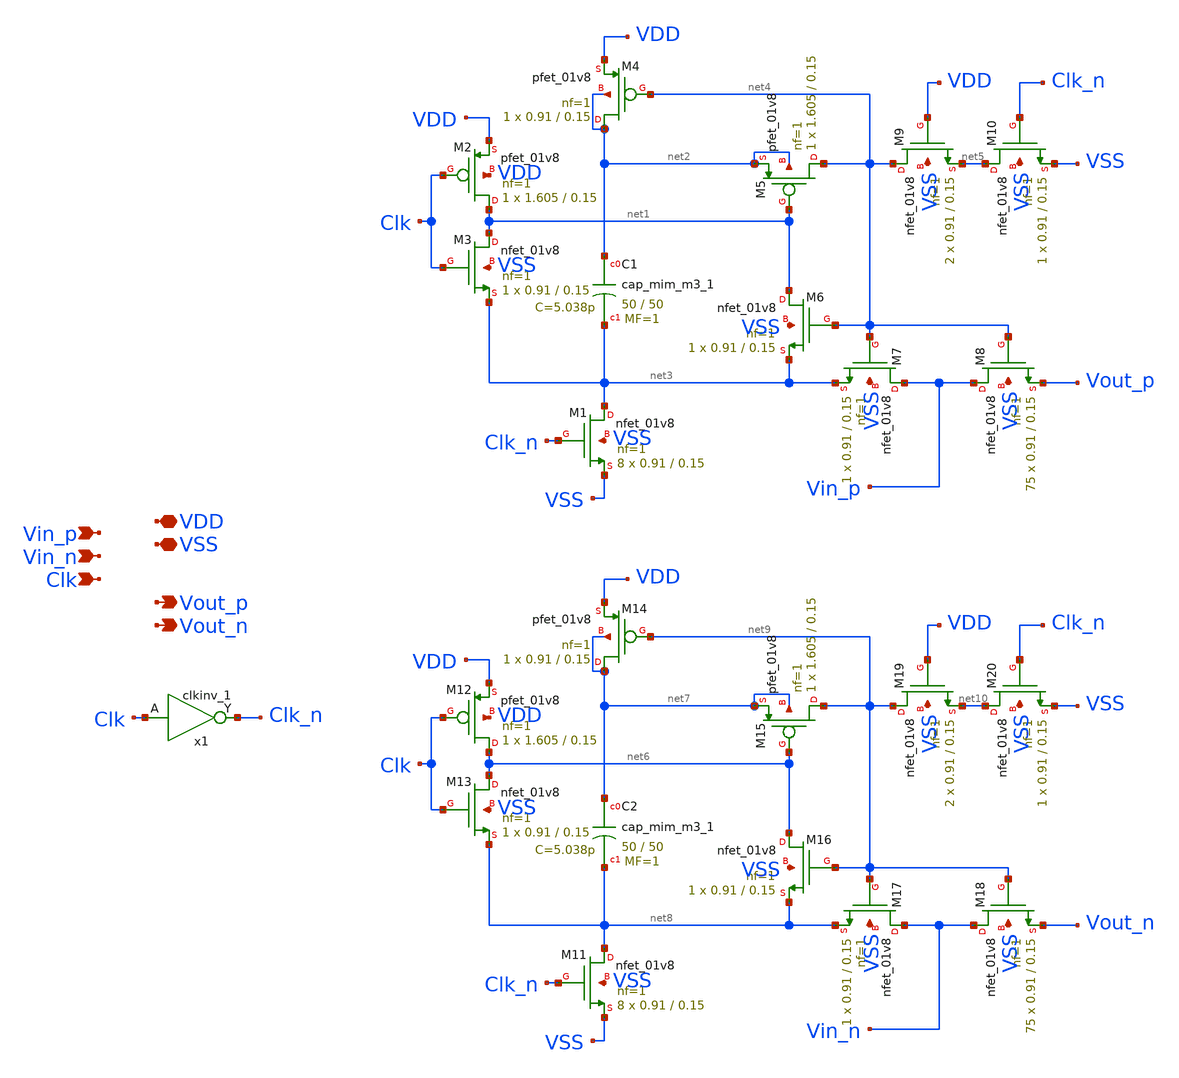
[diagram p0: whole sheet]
** sch_path: xschem/src/bootstrapped_sampling_switch/bootstrapped_sampling_switch.sch
**.subckt bootstrapped_sampling_switch VDD Vin_p Vout_p VSS Vout_n Vin_n Clk
*.iopin VDD
*.ipin Vin_p
*.opin Vout_p
*.iopin VSS
*.opin Vout_n
*.ipin Vin_n
*.ipin Clk
XM1 net3 Clk_n VSS VSS sky130_fd_pr__nfet_01v8 L=0.15 W=0.91 nf=1 ad='int((nf+1)/2) * W/nf * 0.29' as='int((nf+2)/2) * W/nf * 0.29'
+ pd='2*int((nf+1)/2) * (W/nf + 0.29)' ps='2*int((nf+2)/2) * (W/nf + 0.29)' nrd='0.29 / W' nrs='0.29 / W'
+ sa=0 sb=0 sd=0 mult=8 m=8
XM2 net1 Clk VDD VDD sky130_fd_pr__pfet_01v8 L=0.15 W=1.605 nf=1 ad='int((nf+1)/2) * W/nf * 0.29' as='int((nf+2)/2) * W/nf * 0.29'
+ pd='2*int((nf+1)/2) * (W/nf + 0.29)' ps='2*int((nf+2)/2) * (W/nf + 0.29)' nrd='0.29 / W' nrs='0.29 / W'
+ sa=0 sb=0 sd=0 mult=1 m=1
XM3 net1 Clk net3 VSS sky130_fd_pr__nfet_01v8 L=0.15 W=0.91 nf=1 ad='int((nf+1)/2) * W/nf * 0.29' as='int((nf+2)/2) * W/nf * 0.29'
+ pd='2*int((nf+1)/2) * (W/nf + 0.29)' ps='2*int((nf+2)/2) * (W/nf + 0.29)' nrd='0.29 / W' nrs='0.29 / W'
+ sa=0 sb=0 sd=0 mult=1 m=1
XC1 net2 net3 sky130_fd_pr__cap_mim_m3_1 W=50 L=50 MF=1 m=1
XM4 net2 net4 VDD net2 sky130_fd_pr__pfet_01v8 L=0.15 W=0.91 nf=1 ad='int((nf+1)/2) * W/nf * 0.29' as='int((nf+2)/2) * W/nf * 0.29'
+ pd='2*int((nf+1)/2) * (W/nf + 0.29)' ps='2*int((nf+2)/2) * (W/nf + 0.29)' nrd='0.29 / W' nrs='0.29 / W'
+ sa=0 sb=0 sd=0 mult=1 m=1
XM5 net4 net1 net2 net2 sky130_fd_pr__pfet_01v8 L=0.15 W=1.605 nf=1 ad='int((nf+1)/2) * W/nf * 0.29'
+ as='int((nf+2)/2) * W/nf * 0.29' pd='2*int((nf+1)/2) * (W/nf + 0.29)' ps='2*int((nf+2)/2) * (W/nf + 0.29)'
+ nrd='0.29 / W' nrs='0.29 / W' sa=0 sb=0 sd=0 mult=1 m=1
XM6 net1 net4 net3 VSS sky130_fd_pr__nfet_01v8 L=0.15 W=0.91 nf=1 ad='int((nf+1)/2) * W/nf * 0.29' as='int((nf+2)/2) * W/nf * 0.29'
+ pd='2*int((nf+1)/2) * (W/nf + 0.29)' ps='2*int((nf+2)/2) * (W/nf + 0.29)' nrd='0.29 / W' nrs='0.29 / W'
+ sa=0 sb=0 sd=0 mult=1 m=1
XM7 Vin_p net4 net3 VSS sky130_fd_pr__nfet_01v8 L=0.15 W=0.91 nf=1 ad='int((nf+1)/2) * W/nf * 0.29' as='int((nf+2)/2) * W/nf * 0.29'
+ pd='2*int((nf+1)/2) * (W/nf + 0.29)' ps='2*int((nf+2)/2) * (W/nf + 0.29)' nrd='0.29 / W' nrs='0.29 / W'
+ sa=0 sb=0 sd=0 mult=1 m=1
XM8 Vin_p net4 Vout_p VSS sky130_fd_pr__nfet_01v8 L=0.15 W=0.91 nf=1 ad='int((nf+1)/2) * W/nf * 0.29'
+ as='int((nf+2)/2) * W/nf * 0.29' pd='2*int((nf+1)/2) * (W/nf + 0.29)' ps='2*int((nf+2)/2) * (W/nf + 0.29)'
+ nrd='0.29 / W' nrs='0.29 / W' sa=0 sb=0 sd=0 mult=75 m=75
XM9 net4 VDD net5 VSS sky130_fd_pr__nfet_01v8 L=0.15 W=0.91 nf=1 ad='int((nf+1)/2) * W/nf * 0.29' as='int((nf+2)/2) * W/nf * 0.29'
+ pd='2*int((nf+1)/2) * (W/nf + 0.29)' ps='2*int((nf+2)/2) * (W/nf + 0.29)' nrd='0.29 / W' nrs='0.29 / W'
+ sa=0 sb=0 sd=0 mult=2 m=2
XM10 net5 Clk_n VSS VSS sky130_fd_pr__nfet_01v8 L=0.15 W=0.91 nf=1 ad='int((nf+1)/2) * W/nf * 0.29' as='int((nf+2)/2) * W/nf * 0.29'
+ pd='2*int((nf+1)/2) * (W/nf + 0.29)' ps='2*int((nf+2)/2) * (W/nf + 0.29)' nrd='0.29 / W' nrs='0.29 / W'
+ sa=0 sb=0 sd=0 mult=1 m=1
x1 Clk VSS VSS VDD VDD Clk_n sky130_fd_sc_hd__clkinv_1
XM11 net8 Clk_n VSS VSS sky130_fd_pr__nfet_01v8 L=0.15 W=0.91 nf=1 ad='int((nf+1)/2) * W/nf * 0.29' as='int((nf+2)/2) * W/nf * 0.29'
+ pd='2*int((nf+1)/2) * (W/nf + 0.29)' ps='2*int((nf+2)/2) * (W/nf + 0.29)' nrd='0.29 / W' nrs='0.29 / W'
+ sa=0 sb=0 sd=0 mult=8 m=8
XM12 net6 Clk VDD VDD sky130_fd_pr__pfet_01v8 L=0.15 W=1.605 nf=1 ad='int((nf+1)/2) * W/nf * 0.29' as='int((nf+2)/2) * W/nf * 0.29'
+ pd='2*int((nf+1)/2) * (W/nf + 0.29)' ps='2*int((nf+2)/2) * (W/nf + 0.29)' nrd='0.29 / W' nrs='0.29 / W'
+ sa=0 sb=0 sd=0 mult=1 m=1
XM13 net6 Clk net8 VSS sky130_fd_pr__nfet_01v8 L=0.15 W=0.91 nf=1 ad='int((nf+1)/2) * W/nf * 0.29' as='int((nf+2)/2) * W/nf * 0.29'
+ pd='2*int((nf+1)/2) * (W/nf + 0.29)' ps='2*int((nf+2)/2) * (W/nf + 0.29)' nrd='0.29 / W' nrs='0.29 / W'
+ sa=0 sb=0 sd=0 mult=1 m=1
XC2 net7 net8 sky130_fd_pr__cap_mim_m3_1 W=50 L=50 MF=1 m=1
XM14 net7 net9 VDD net7 sky130_fd_pr__pfet_01v8 L=0.15 W=0.91 nf=1 ad='int((nf+1)/2) * W/nf * 0.29' as='int((nf+2)/2) * W/nf * 0.29'
+ pd='2*int((nf+1)/2) * (W/nf + 0.29)' ps='2*int((nf+2)/2) * (W/nf + 0.29)' nrd='0.29 / W' nrs='0.29 / W'
+ sa=0 sb=0 sd=0 mult=1 m=1
XM15 net9 net6 net7 net7 sky130_fd_pr__pfet_01v8 L=0.15 W=1.605 nf=1 ad='int((nf+1)/2) * W/nf * 0.29'
+ as='int((nf+2)/2) * W/nf * 0.29' pd='2*int((nf+1)/2) * (W/nf + 0.29)' ps='2*int((nf+2)/2) * (W/nf + 0.29)'
+ nrd='0.29 / W' nrs='0.29 / W' sa=0 sb=0 sd=0 mult=1 m=1
XM16 net6 net9 net8 VSS sky130_fd_pr__nfet_01v8 L=0.15 W=0.91 nf=1 ad='int((nf+1)/2) * W/nf * 0.29' as='int((nf+2)/2) * W/nf * 0.29'
+ pd='2*int((nf+1)/2) * (W/nf + 0.29)' ps='2*int((nf+2)/2) * (W/nf + 0.29)' nrd='0.29 / W' nrs='0.29 / W'
+ sa=0 sb=0 sd=0 mult=1 m=1
XM17 Vin_n net9 net8 VSS sky130_fd_pr__nfet_01v8 L=0.15 W=0.91 nf=1 ad='int((nf+1)/2) * W/nf * 0.29'
+ as='int((nf+2)/2) * W/nf * 0.29' pd='2*int((nf+1)/2) * (W/nf + 0.29)' ps='2*int((nf+2)/2) * (W/nf + 0.29)'
+ nrd='0.29 / W' nrs='0.29 / W' sa=0 sb=0 sd=0 mult=1 m=1
XM18 Vin_n net9 Vout_n VSS sky130_fd_pr__nfet_01v8 L=0.15 W=0.91 nf=1 ad='int((nf+1)/2) * W/nf * 0.29'
+ as='int((nf+2)/2) * W/nf * 0.29' pd='2*int((nf+1)/2) * (W/nf + 0.29)' ps='2*int((nf+2)/2) * (W/nf + 0.29)'
+ nrd='0.29 / W' nrs='0.29 / W' sa=0 sb=0 sd=0 mult=75 m=75
XM19 net9 VDD net10 VSS sky130_fd_pr__nfet_01v8 L=0.15 W=0.91 nf=1 ad='int((nf+1)/2) * W/nf * 0.29' as='int((nf+2)/2) * W/nf * 0.29'
+ pd='2*int((nf+1)/2) * (W/nf + 0.29)' ps='2*int((nf+2)/2) * (W/nf + 0.29)' nrd='0.29 / W' nrs='0.29 / W'
+ sa=0 sb=0 sd=0 mult=2 m=2
XM20 net10 Clk_n VSS VSS sky130_fd_pr__nfet_01v8 L=0.15 W=0.91 nf=1 ad='int((nf+1)/2) * W/nf * 0.29'
+ as='int((nf+2)/2) * W/nf * 0.29' pd='2*int((nf+1)/2) * (W/nf + 0.29)' ps='2*int((nf+2)/2) * (W/nf + 0.29)'
+ nrd='0.29 / W' nrs='0.29 / W' sa=0 sb=0 sd=0 mult=1 m=1
**.ends
.end
